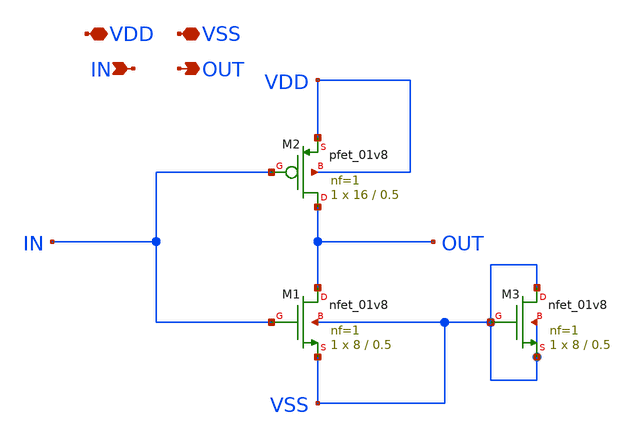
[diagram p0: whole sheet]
** sch_path: Xschem/PLL_TOP_Schematics/INV_1.sch
**.subckt INV_1 VDD VSS IN OUT
*.iopin VDD
*.iopin VSS
*.ipin IN
*.opin OUT
XM1 OUT IN VSS VSS sky130_fd_pr__nfet_01v8 L=0.5 W=8 nf=1 ad='int((nf+1)/2) * W/nf * 0.29' as='int((nf+2)/2) * W/nf * 0.29'
+ pd='2*int((nf+1)/2) * (W/nf + 0.29)' ps='2*int((nf+2)/2) * (W/nf + 0.29)' nrd='0.29 / W' nrs='0.29 / W'
+ sa=0 sb=0 sd=0 mult=1 m=1
XM2 OUT IN VDD VDD sky130_fd_pr__pfet_01v8 L=0.5 W=16 nf=1 ad='int((nf+1)/2) * W/nf * 0.29' as='int((nf+2)/2) * W/nf * 0.29'
+ pd='2*int((nf+1)/2) * (W/nf + 0.29)' ps='2*int((nf+2)/2) * (W/nf + 0.29)' nrd='0.29 / W' nrs='0.29 / W'
+ sa=0 sb=0 sd=0 mult=1 m=1
XM3 VSS VSS VSS VSS sky130_fd_pr__nfet_01v8 L=0.5 W=8 nf=1 ad='int((nf+1)/2) * W/nf * 0.29' as='int((nf+2)/2) * W/nf * 0.29'
+ pd='2*int((nf+1)/2) * (W/nf + 0.29)' ps='2*int((nf+2)/2) * (W/nf + 0.29)' nrd='0.29 / W' nrs='0.29 / W'
+ sa=0 sb=0 sd=0 mult=1 m=1
**.ends
.end
